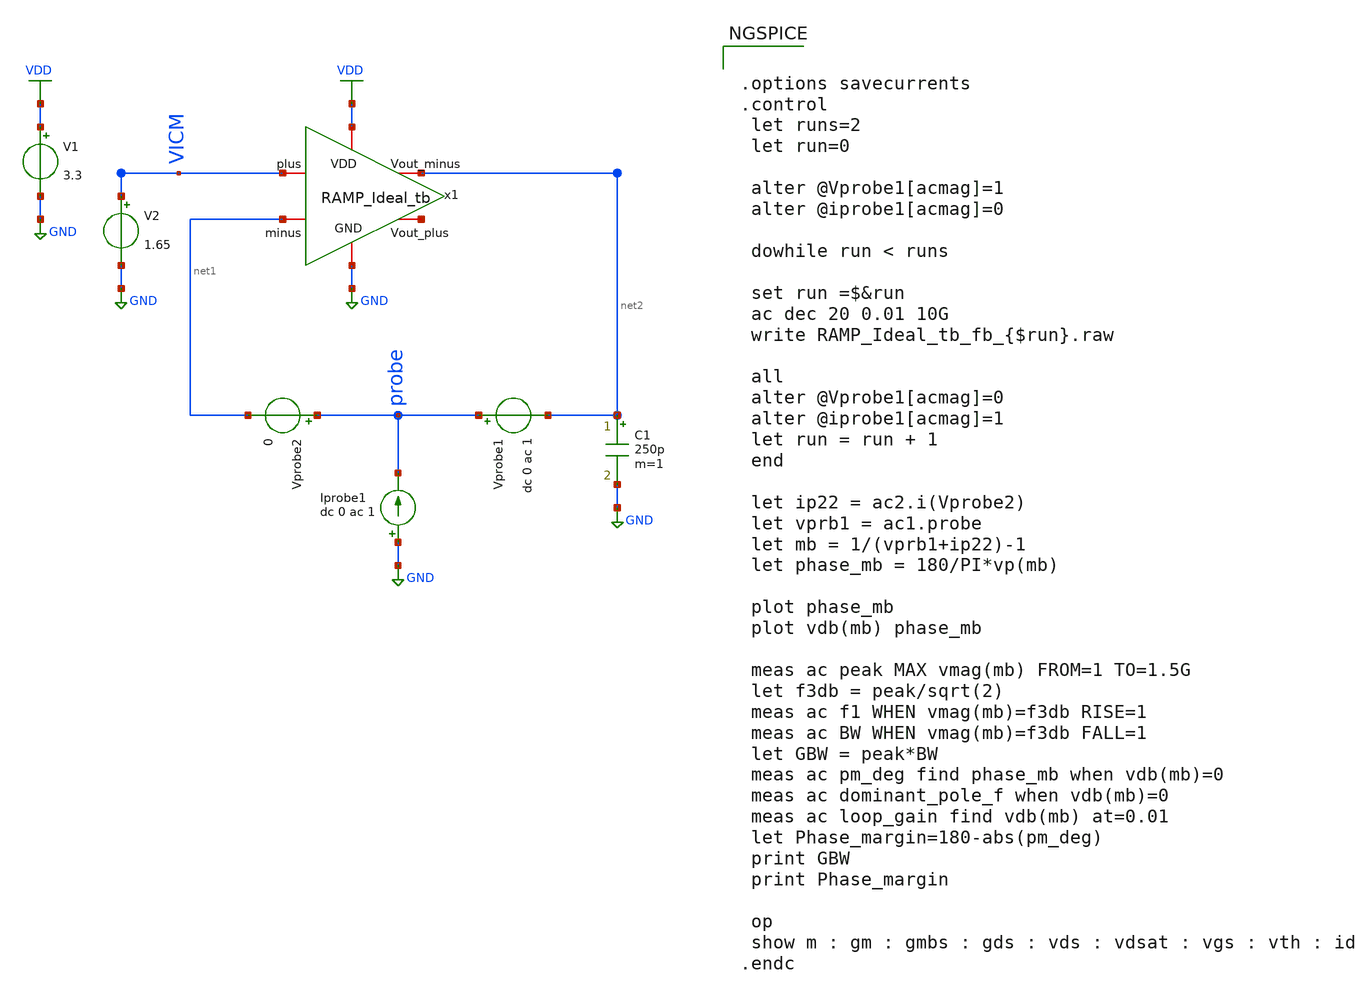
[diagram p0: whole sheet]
** sch_path: Design_Files/RAMP_Ideal/RAMP_Ideal_tb_fb.sch
**.subckt RAMP_Ideal_tb_fb
x1 VDD VICM net2 net3 net1 GND RAMP_Ideal_tb
V1 VDD GND 3.3
V2 VICM GND 1.65
C1 net2 GND 250p m=1
Vprobe2 probe net1 0
Vprobe1 probe net2 dc 0 ac 1
Iprobe1 GND probe dc 0 ac 1
**** begin user architecture code


.options savecurrents
.control
 let runs=2
 let run=0

 alter @Vprobe1[acmag]=1
 alter @iprobe1[acmag]=0

 dowhile run < runs

 set run =$&run
 ac dec 20 0.01 10G
 write RAMP_Ideal_tb_fb_{$run}.raw

 all
 alter @Vprobe1[acmag]=0
 alter @iprobe1[acmag]=1
 let run = run + 1
 end

 let ip22 = ac2.i(Vprobe2)
 let vprb1 = ac1.probe
 let mb = 1/(vprb1+ip22)-1
 let phase_mb = 180/PI*vp(mb)

 plot phase_mb
 plot vdb(mb) phase_mb

 meas ac peak MAX vmag(mb) FROM=1 TO=1.5G
 let f3db = peak/sqrt(2)
 meas ac f1 WHEN vmag(mb)=f3db RISE=1
 meas ac BW WHEN vmag(mb)=f3db FALL=1
 let GBW = peak*BW
 meas ac pm_deg find phase_mb when vdb(mb)=0
 meas ac dominant_pole_f when vdb(mb)=0
 meas ac loop_gain find vdb(mb) at=0.01
 let Phase_margin=180-abs(pm_deg)
 print GBW
 print Phase_margin

 op
 show m : gm : gmbs : gds : vds : vdsat : vgs : vth : id
.endc




.save @m.xm1.m0[gm]
.save @m.xm1.m0[id]
.save @m.xm1.m0[vth]
.save @m.xm1.m0[gds]
.save @m.xm1.m0[cgg]
.save @m.xm1.m0[cgs]
.save @m.xm1.m0[cgd]
.save @m.xm2.m0[gm]
.save @m.xm2.m0[id]
.save @m.xm2.m0[vth]
.save @m.xm2.m0[gds]
.save @m.xm2.m0[cgg]
.save @m.xm2.m0[cgs]
.save @m.xm2.m0[cgd]
.save @m.xm3.m0[gm]
.save @m.xm3.m0[id]
.save @m.xm3.m0[vth]
.save @m.xm3.m0[vds]
.save @m.xm3.m0[gds]
.save @m.xm3.m0[cgg]
.save @m.xm3.m0[cgs]
.save @m.xm3.m0[cgd]
.save @m.xm4.m0[gm]
.save @m.xm4.m0[id]
.save @m.xm4.m0[vth]
.save @m.xm4.m0[vds]
.save @m.xm4.m0[gds]
.save @m.xm4.m0[cgg]
.save @m.xm4.m0[cgs]
.save @m.xm4.m0[cgd]



.lib /foss/pdks/volare/gf180mcu/versions/0fe599b2afb6708d281543108caf8310912f54af/gf180mcuD/libs.tech/ngspice/sm141064.ngspice typical
.include /foss/pdks/volare/gf180mcu/versions/0fe599b2afb6708d281543108caf8310912f54af/gf180mcuD/libs.tech/ngspice/design.ngspice
.lib /foss/pdks/volare/gf180mcu/versions/0fe599b2afb6708d281543108caf8310912f54af/gf180mcuD/libs.tech/ngspice/sm141064.ngspice res_statistical

**.include $::180MCU_MODELS/design.ngspice
**.lib $::180MCU_MODELS/sm141064.ngspice typical
**.lib $::180MCU_MODELS/sm141064.ngspice res_typical
* .lib $::180MCU_MODELS/sm141064.ngspice res_statistical
*.include $::180MCU_MODELS/design.ngspice
*.lib $::180MCU_MODELS/sm141064.ngspice typical


**** end user architecture code
**.ends

* expanding   symbol:  chipathon/RAMP_Ideal/RAMP_Ideal_tb.sym # of pins=6
** sym_path: Design_Files/RAMP_Ideal/RAMP_Ideal_tb.sym
** sch_path: Design_Files/RAMP_Ideal/RAMP_Ideal_tb.sch
.subckt RAMP_Ideal_tb VDD plus Vout_minus Vout_plus minus GND
*.iopin plus
*.iopin minus
*.iopin Vout_minus
*.iopin Vout_plus
*.iopin VDD
*.iopin GND
XM6 Vout_minus net2 VDD VDD pfet_03v3 L=0.5u W=15.375u nf=1 ad='int((nf+1)/2) * W/nf * 0.18u' as='int((nf+2)/2) * W/nf * 0.18u'
+ pd='2*int((nf+1)/2) * (W/nf + 0.18u)' ps='2*int((nf+2)/2) * (W/nf + 0.18u)' nrd='0.18u / W' nrs='0.18u / W'
+ sa=0 sb=0 sd=0 m=8
XM7 Vout_minus net3 GND GND nfet_03v3 L=0.5u W=5u nf=1 ad='int((nf+1)/2) * W/nf * 0.18u' as='int((nf+2)/2) * W/nf * 0.18u'
+ pd='2*int((nf+1)/2) * (W/nf + 0.18u)' ps='2*int((nf+2)/2) * (W/nf + 0.18u)' nrd='0.18u / W' nrs='0.18u / W'
+ sa=0 sb=0 sd=0 m=8
E1 net2 net1 VGP_bias VCM 1
E2 net3 net1 VGN_bias VCM 1
G1 net1 VCM net4 VCM 3.99269m
R1 net1 VCM 254.648 m=1
C1 net1 VCM 50f m=1
R2 net4 VCM 254.648 m=1
C2 net4 VCM 50f m=1
G2 net4 VCM plus VCM 7.8539m
XM1 VGN_bias VGN_bias GND GND nfet_03v3 L=0.5u W=5u nf=1 ad='int((nf+1)/2) * W/nf * 0.18u' as='int((nf+2)/2) * W/nf * 0.18u'
+ pd='2*int((nf+1)/2) * (W/nf + 0.18u)' ps='2*int((nf+2)/2) * (W/nf + 0.18u)' nrd='0.18u / W' nrs='0.18u / W'
+ sa=0 sb=0 sd=0 m=8
I0 VDD VGN_bias 10u
XM2 VGP_bias VGP_bias VDD VDD pfet_03v3 L=0.5u W=15.375u nf=1 ad='int((nf+1)/2) * W/nf * 0.18u' as='int((nf+2)/2) * W/nf * 0.18u'
+ pd='2*int((nf+1)/2) * (W/nf + 0.18u)' ps='2*int((nf+2)/2) * (W/nf + 0.18u)' nrd='0.18u / W' nrs='0.18u / W'
+ sa=0 sb=0 sd=0 m=8
I1 VGP_bias GND 10u
XM3 Vout_plus net5 VDD VDD pfet_03v3 L=0.5u W=15.375u nf=1 ad='int((nf+1)/2) * W/nf * 0.18u' as='int((nf+2)/2) * W/nf * 0.18u'
+ pd='2*int((nf+1)/2) * (W/nf + 0.18u)' ps='2*int((nf+2)/2) * (W/nf + 0.18u)' nrd='0.18u / W' nrs='0.18u / W'
+ sa=0 sb=0 sd=0 m=8
XM4 Vout_plus net6 GND GND nfet_03v3 L=0.5u W=5u nf=1 ad='int((nf+1)/2) * W/nf * 0.18u' as='int((nf+2)/2) * W/nf * 0.18u'
+ pd='2*int((nf+1)/2) * (W/nf + 0.18u)' ps='2*int((nf+2)/2) * (W/nf + 0.18u)' nrd='0.18u / W' nrs='0.18u / W'
+ sa=0 sb=0 sd=0 m=8
E3 net5 VCM VGP_bias VCM 1
E4 net6 VCM VGN_bias VCM 1
.ends

.GLOBAL GND
.GLOBAL VDD
.end
